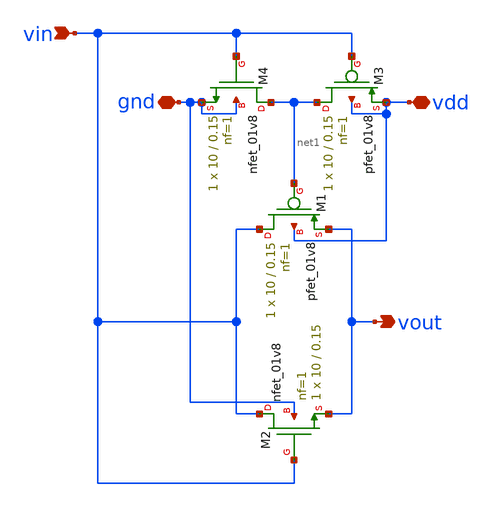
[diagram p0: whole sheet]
** sch_path: switch/transmission_gate.sch
**.subckt transmission_gate gnd vdd vout vin
*.iopin gnd
*.iopin vdd
*.opin vout
*.ipin vin
XM1 vin net1 vout vdd sky130_fd_pr__pfet_01v8 L=0.15 W=10 nf=1 ad='int((nf+1)/2) * W/nf * 0.29' as='int((nf+2)/2) * W/nf * 0.29'
+ pd='2*int((nf+1)/2) * (W/nf + 0.29)' ps='2*int((nf+2)/2) * (W/nf + 0.29)' nrd='0.29 / W' nrs='0.29 / W'
+ sa=0 sb=0 sd=0 mult=1 m=1
XM2 vin vin vout gnd sky130_fd_pr__nfet_01v8 L=0.15 W=10 nf=1 ad='int((nf+1)/2) * W/nf * 0.29' as='int((nf+2)/2) * W/nf * 0.29'
+ pd='2*int((nf+1)/2) * (W/nf + 0.29)' ps='2*int((nf+2)/2) * (W/nf + 0.29)' nrd='0.29 / W' nrs='0.29 / W'
+ sa=0 sb=0 sd=0 mult=1 m=1
XM3 net1 vin vdd vdd sky130_fd_pr__pfet_01v8 L=0.15 W=10 nf=1 ad='int((nf+1)/2) * W/nf * 0.29' as='int((nf+2)/2) * W/nf * 0.29'
+ pd='2*int((nf+1)/2) * (W/nf + 0.29)' ps='2*int((nf+2)/2) * (W/nf + 0.29)' nrd='0.29 / W' nrs='0.29 / W'
+ sa=0 sb=0 sd=0 mult=1 m=1
XM4 net1 vin gnd gnd sky130_fd_pr__nfet_01v8 L=0.15 W=10 nf=1 ad='int((nf+1)/2) * W/nf * 0.29' as='int((nf+2)/2) * W/nf * 0.29'
+ pd='2*int((nf+1)/2) * (W/nf + 0.29)' ps='2*int((nf+2)/2) * (W/nf + 0.29)' nrd='0.29 / W' nrs='0.29 / W'
+ sa=0 sb=0 sd=0 mult=1 m=1
**.ends
.end
